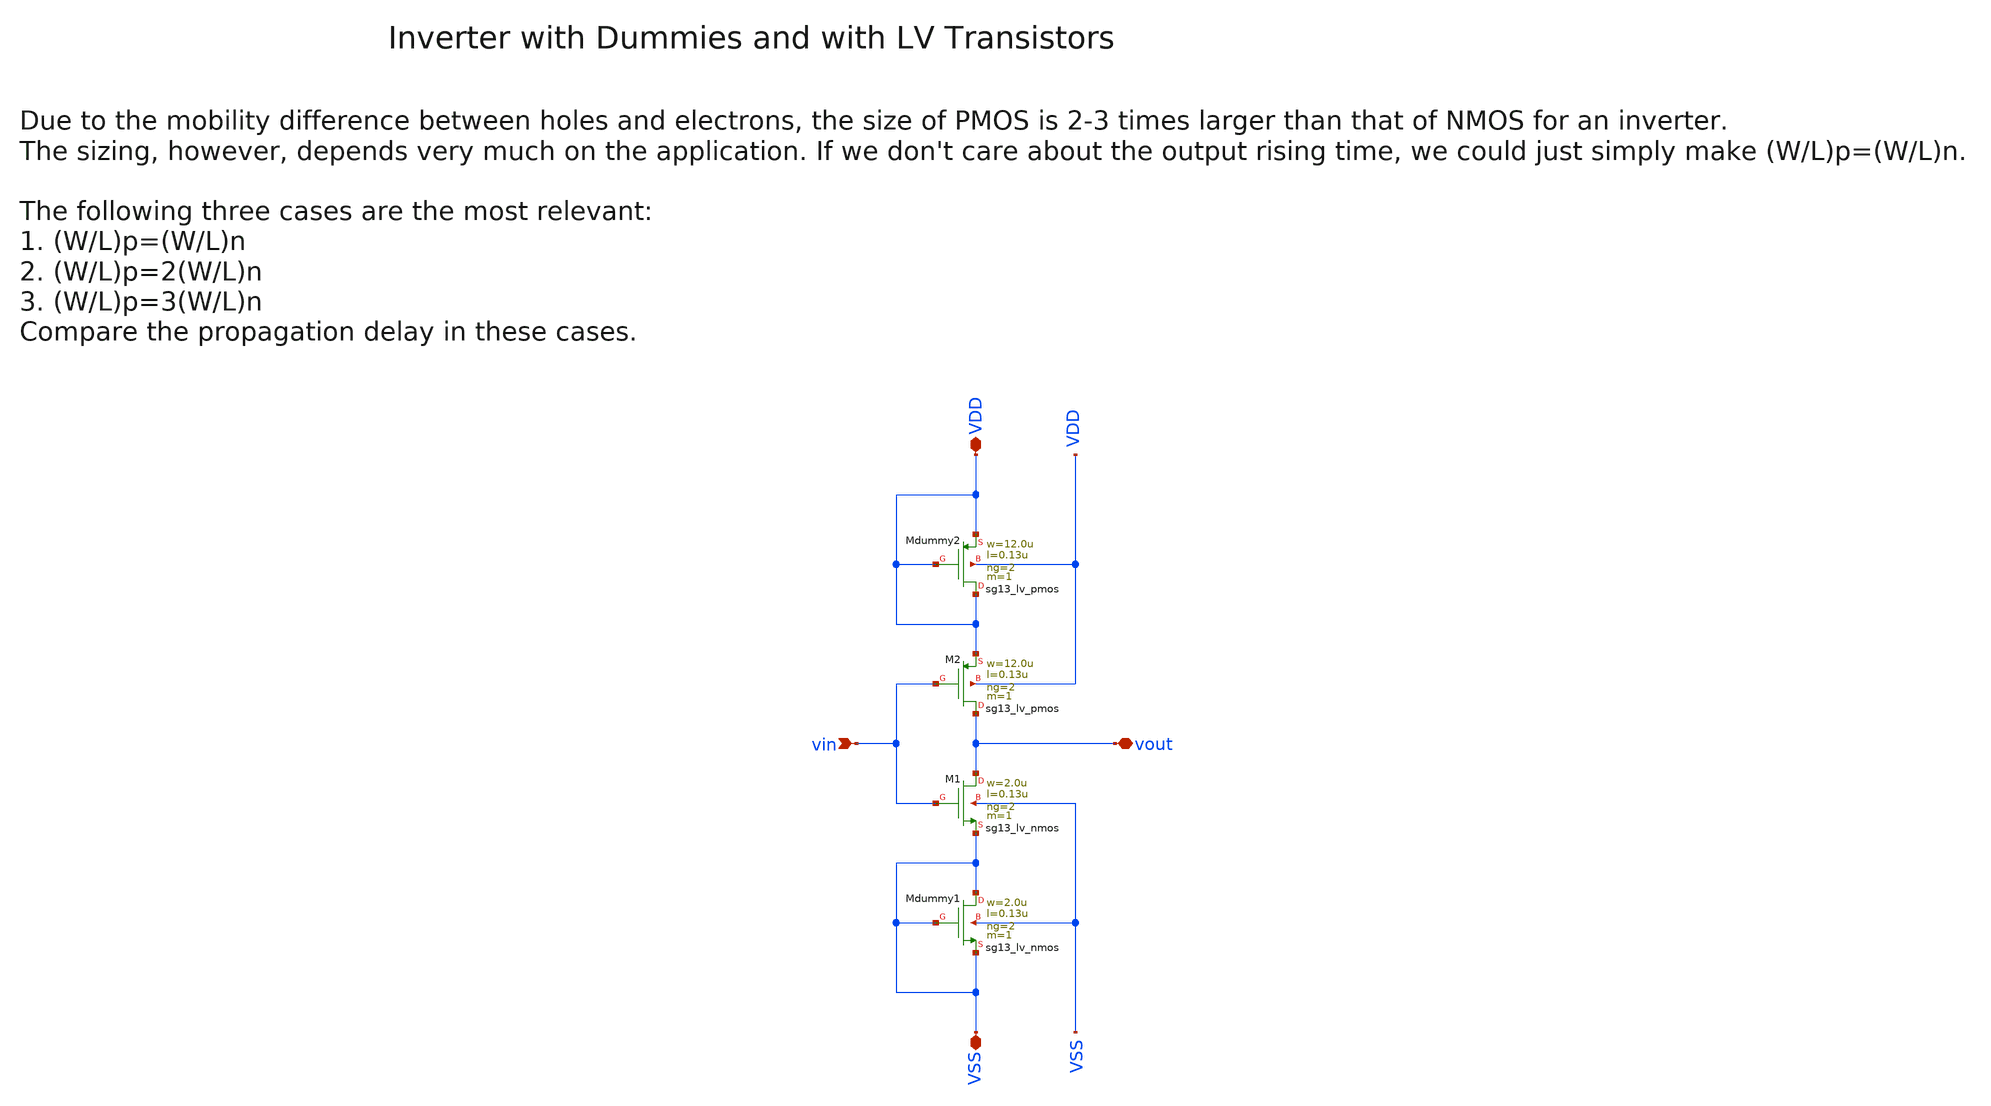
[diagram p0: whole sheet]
** sch_path: ihp130/macros/iqmod/schematic/xschem/iqmod_mfb_lpf_ota_core_spdt_switch_inv.sch
**.subckt iqmod_mfb_lpf_ota_core_spdt_switch_inv vin VDD VSS vout
*.ipin vin
*.iopin VDD
*.iopin VSS
*.iopin vout
XM1 vout vin VSS VSS sg13_lv_nmos w=2.0u l=0.13u ng=2 m=1 mm_ok=1
XM2 vout vin VDD VDD sg13_lv_pmos w=12.0u l=0.13u ng=2 m=1 mm_ok=1
XMdummy1 VSS VSS VSS VSS sg13_lv_nmos w=2.0u l=0.13u ng=2 m=1 mm_ok=1
XMdummy2 VDD VDD VDD VDD sg13_lv_pmos w=12.0u l=0.13u ng=2 m=1 mm_ok=1
**.ends
.end
